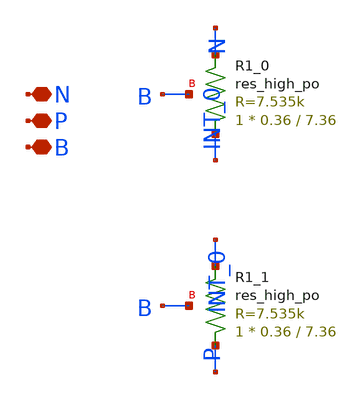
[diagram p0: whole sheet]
** sch_path: design/REY_TR_SKY130A/REYTR_RES2.sch
**.subckt REYTR_RES2 N P B
*.iopin N
*.iopin P
*.iopin B
XR1_0 INT_0 N B sky130_fd_pr__res_high_po W=0.36 L=7.36 mult=1 m=1
XR1_1 P INT_0 B sky130_fd_pr__res_high_po W=0.36 L=7.36 mult=1 m=1
**.ends
.end
